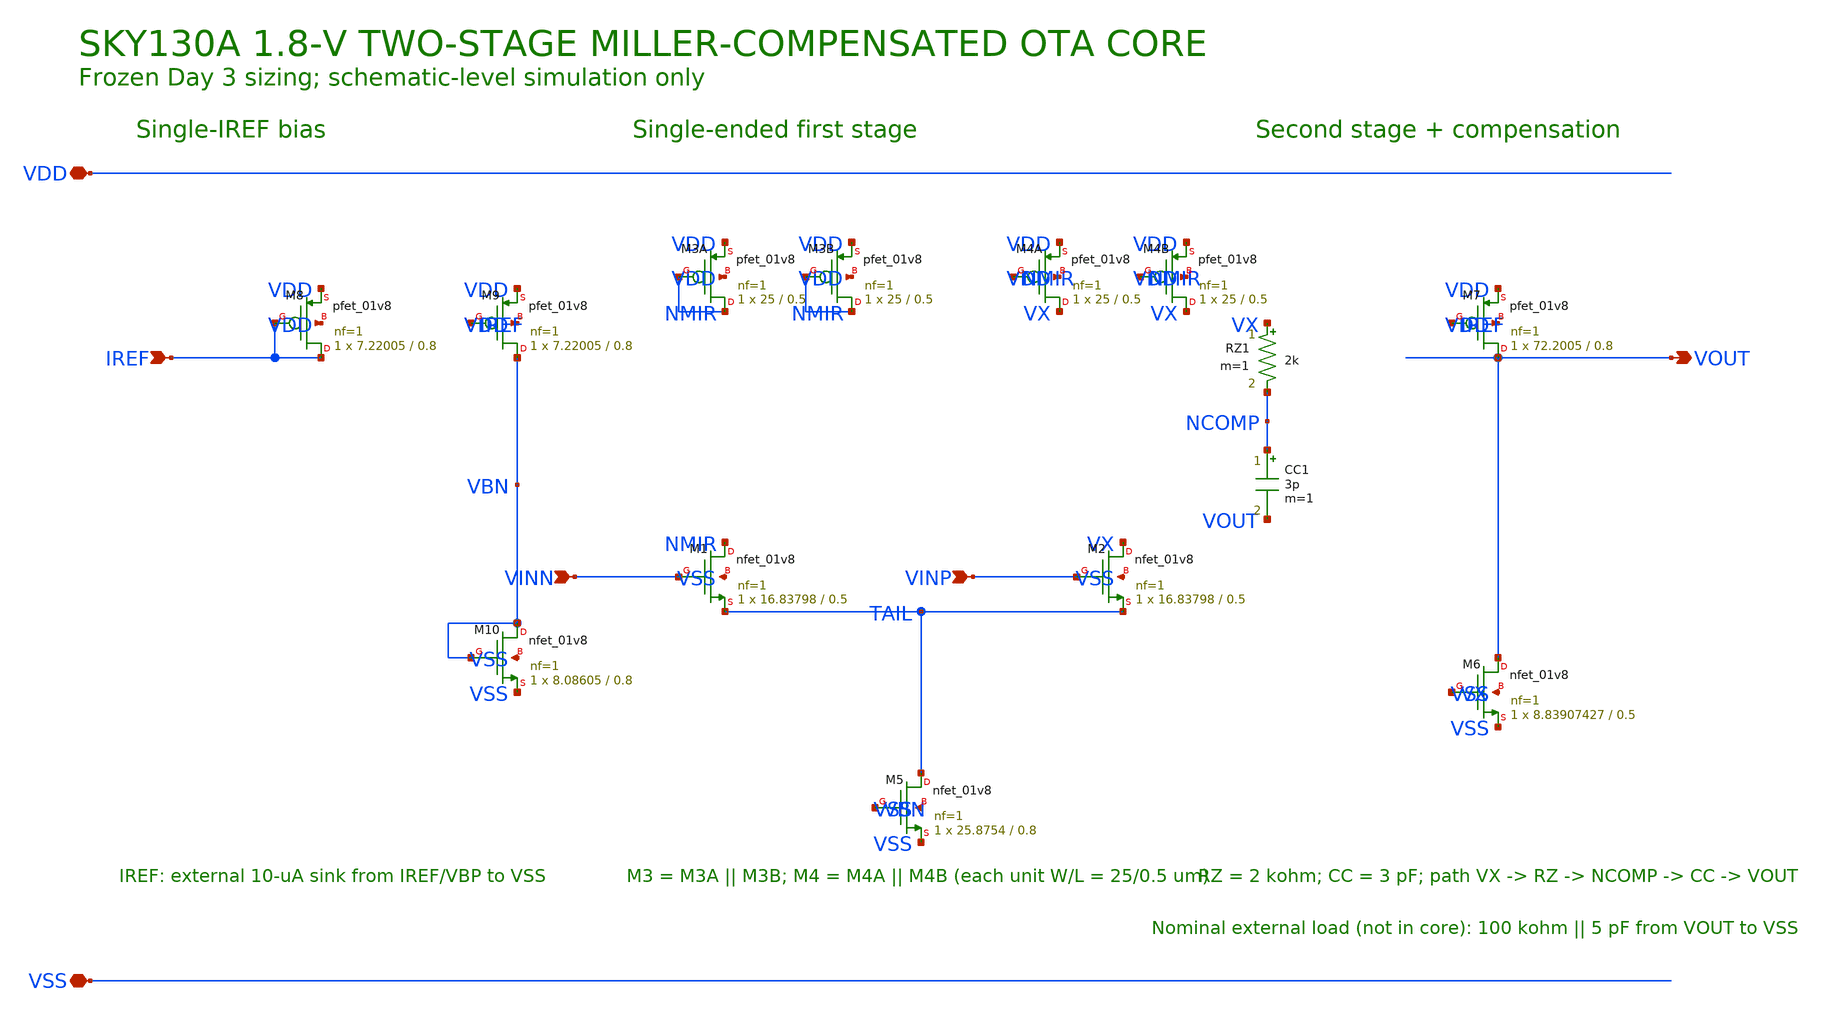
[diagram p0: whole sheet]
** sch_path: schematics/two_stage_ota.sch
**.subckt two_stage_ota VINP VINN VOUT VDD VSS IREF
*.ipin VINP
*.ipin VINN
*.opin VOUT
*.iopin VDD
*.iopin VSS
*.ipin IREF
XM8 IREF IREF VDD VDD sky130_fd_pr__pfet_01v8 L=0.8 W=7.22005 nf=1 ad='int((nf+1)/2) * W/nf * 0.29' as='int((nf+2)/2) * W/nf * 0.29'
+ pd='2*int((nf+1)/2) * (W/nf + 0.29)' ps='2*int((nf+2)/2) * (W/nf + 0.29)' nrd='0.29 / W' nrs='0.29 / W'
+ sa=0 sb=0 sd=0 mult=1 m=1
XM9 VBN IREF VDD VDD sky130_fd_pr__pfet_01v8 L=0.8 W=7.22005 nf=1 ad='int((nf+1)/2) * W/nf * 0.29' as='int((nf+2)/2) * W/nf * 0.29'
+ pd='2*int((nf+1)/2) * (W/nf + 0.29)' ps='2*int((nf+2)/2) * (W/nf + 0.29)' nrd='0.29 / W' nrs='0.29 / W'
+ sa=0 sb=0 sd=0 mult=1 m=1
XM10 VBN VBN VSS VSS sky130_fd_pr__nfet_01v8 L=0.8 W=8.08605 nf=1 ad='int((1 + 1)/2) * 8.08605 / 1 * 0.29'
+ as='int((1 + 2)/2) * 8.08605 / 1 * 0.29' pd='2*int((1 + 1)/2) * (8.08605 / 1 + 0.29)' ps='2*int((1 + 2)/2) * (8.08605 / 1 + 0.29)'
+ nrd='0.29 / 8.08605 ' nrs='0.29 / 8.08605 ' sa=0 sb=0 sd=0 mult=1 m=1
XM3A NMIR NMIR VDD VDD sky130_fd_pr__pfet_01v8 L=0.5 W=25 nf=1 ad='int((nf+1)/2) * W/nf * 0.29' as='int((nf+2)/2) * W/nf * 0.29'
+ pd='2*int((nf+1)/2) * (W/nf + 0.29)' ps='2*int((nf+2)/2) * (W/nf + 0.29)' nrd='0.29 / W' nrs='0.29 / W'
+ sa=0 sb=0 sd=0 mult=1 m=1
XM3B NMIR NMIR VDD VDD sky130_fd_pr__pfet_01v8 L=0.5 W=25 nf=1 ad='int((nf+1)/2) * W/nf * 0.29' as='int((nf+2)/2) * W/nf * 0.29'
+ pd='2*int((nf+1)/2) * (W/nf + 0.29)' ps='2*int((nf+2)/2) * (W/nf + 0.29)' nrd='0.29 / W' nrs='0.29 / W'
+ sa=0 sb=0 sd=0 mult=1 m=1
XM4A VX NMIR VDD VDD sky130_fd_pr__pfet_01v8 L=0.5 W=25 nf=1 ad='int((nf+1)/2) * W/nf * 0.29' as='int((nf+2)/2) * W/nf * 0.29'
+ pd='2*int((nf+1)/2) * (W/nf + 0.29)' ps='2*int((nf+2)/2) * (W/nf + 0.29)' nrd='0.29 / W' nrs='0.29 / W'
+ sa=0 sb=0 sd=0 mult=1 m=1
XM4B VX NMIR VDD VDD sky130_fd_pr__pfet_01v8 L=0.5 W=25 nf=1 ad='int((nf+1)/2) * W/nf * 0.29' as='int((nf+2)/2) * W/nf * 0.29'
+ pd='2*int((nf+1)/2) * (W/nf + 0.29)' ps='2*int((nf+2)/2) * (W/nf + 0.29)' nrd='0.29 / W' nrs='0.29 / W'
+ sa=0 sb=0 sd=0 mult=1 m=1
XM1 NMIR VINN TAIL VSS sky130_fd_pr__nfet_01v8 L=0.5 W=16.83798 nf=1 ad='int((1 + 1)/2) * 16.83798 / 1 * 0.29'
+ as='int((1 + 2)/2) * 16.83798 / 1 * 0.29' pd='2*int((1 + 1)/2) * (16.83798 / 1 + 0.29)' ps='2*int((1 + 2)/2) * (16.83798 / 1 + 0.29)'
+ nrd='0.29 / 16.83798 ' nrs='0.29 / 16.83798 ' sa=0 sb=0 sd=0 mult=1 m=1
XM2 VX VINP TAIL VSS sky130_fd_pr__nfet_01v8 L=0.5 W=16.83798 nf=1 ad='int((1 + 1)/2) * 16.83798 / 1 * 0.29'
+ as='int((1 + 2)/2) * 16.83798 / 1 * 0.29' pd='2*int((1 + 1)/2) * (16.83798 / 1 + 0.29)' ps='2*int((1 + 2)/2) * (16.83798 / 1 + 0.29)'
+ nrd='0.29 / 16.83798 ' nrs='0.29 / 16.83798 ' sa=0 sb=0 sd=0 mult=1 m=1
XM5 TAIL VBN VSS VSS sky130_fd_pr__nfet_01v8 L=0.8 W=25.8754 nf=1 ad='int((1 + 1)/2) * 25.8754 / 1 * 0.29'
+ as='int((1 + 2)/2) * 25.8754 / 1 * 0.29' pd='2*int((1 + 1)/2) * (25.8754 / 1 + 0.29)' ps='2*int((1 + 2)/2) * (25.8754 / 1 + 0.29)'
+ nrd='0.29 / 25.8754 ' nrs='0.29 / 25.8754 ' sa=0 sb=0 sd=0 mult=1 m=1
XM7 VOUT IREF VDD VDD sky130_fd_pr__pfet_01v8 L=0.8 W=72.2005 nf=1 ad='int((nf+1)/2) * W/nf * 0.29' as='int((nf+2)/2) * W/nf * 0.29'
+ pd='2*int((nf+1)/2) * (W/nf + 0.29)' ps='2*int((nf+2)/2) * (W/nf + 0.29)' nrd='0.29 / W' nrs='0.29 / W'
+ sa=0 sb=0 sd=0 mult=1 m=1
XM6 VOUT VX VSS VSS sky130_fd_pr__nfet_01v8 L=0.5 W=8.83907427 nf=1 ad='int((1 + 1)/2) * 8.83907427 / 1 * 0.29'
+ as='int((1 + 2)/2) * 8.83907427 / 1 * 0.29' pd='2*int((1 + 1)/2) * (8.83907427 / 1 + 0.29)' ps='2*int((1 + 2)/2) * (8.83907427 / 1 + 0.29)'
+ nrd='0.29 / 8.83907427 ' nrs='0.29 / 8.83907427 ' sa=0 sb=0 sd=0 mult=1 m=1
RZ1 VX NCOMP 2k m=1
CC1 NCOMP VOUT 3p m=1
**.ends
.end
